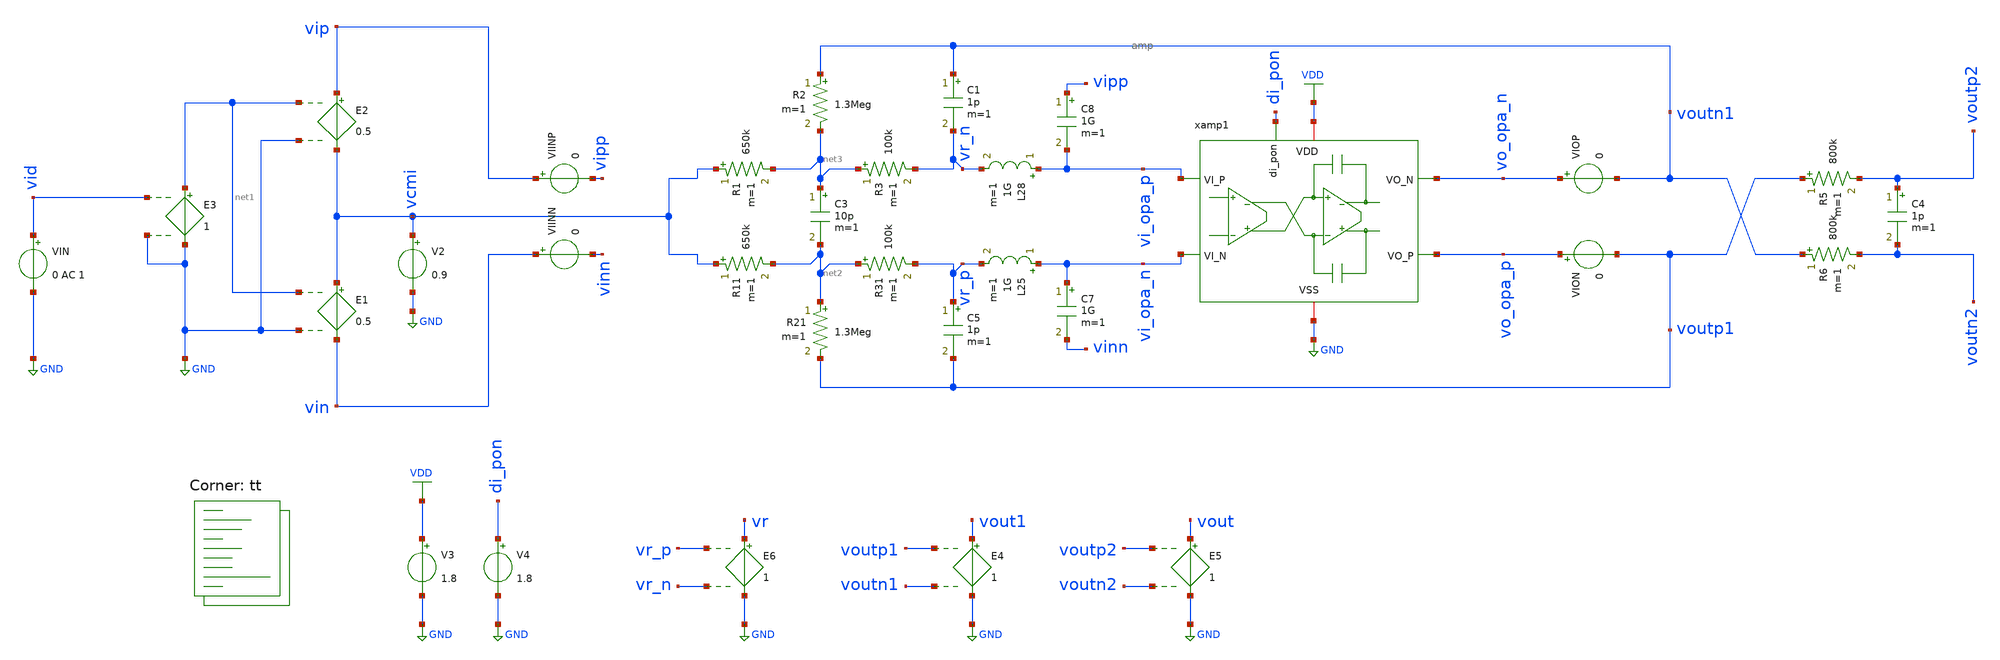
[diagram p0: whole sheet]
** sch_path: xschem/tb_filter_loopgain.sch
**.subckt tb_filter_loopgain
V2 vcmi GND 0.9
E1 vcmi vin net1 GND 0.5
E2 vip vcmi net1 GND 0.5
VIN vid GND 0 AC 1
E3 net1 GND vid GND 1
E4 vout1 GND voutp1 voutn1 1
VIINP vip vipp 0
VIINN vin vinn 0
R1 vcmi net3 650k m=1
R2 voutn1 net3 1.3Meg m=1
R3 net3 vr_n 100k m=1
C1 voutn1 vr_n 1p m=1
C3 net3 net2 10p m=1
R11 vcmi net2 650k m=1
R21 net2 voutp1 1.3Meg m=1
R31 net2 vr_p 100k m=1
C5 vr_p voutp1 1p m=1
E5 vout GND voutp2 voutn2 1
VIOP vo_opa_n voutn1 0
VION vo_opa_p voutp1 0
E6 vr GND vr_p vr_n 1
C7 vi_opa_n vinn 1G m=1
C8 vipp vi_opa_p 1G m=1
L25 vi_opa_n vr_p 1G m=1
L28 vi_opa_p vr_n 1G m=1
xamp1 VDD vi_opa_n vi_opa_p vo_opa_p di_pon vo_opa_n GND amp
V3 VDD GND 1.8
V4 di_pon GND 1.8
C4 voutp2 voutn2 1p m=1
R5 voutp1 voutp2 800k m=1
R6 voutn1 voutn2 800k m=1
**** begin user architecture code
.lib $::SKYWATER_MODELS/sky130.lib.spice tt


.options savecurrents
.options method=gear reltol=.01
.options sparse
.control
save all

let f_sig = 100
let f_min = 10
let f_max = 100G
let f_stop = 5Meg
let tper_sig = 1/f_sig
let tfr_sig = tper_sig/2
let Adc = 10
let beta = 1/Adc
let v_step_o = 0.9
let v_step_i = v_step_o/Adc

let t_rf = 0.1u
let t_step = 50u
let t_delay = 0
let t_per = 2*t_step

let tstep = 0.1*t_rf
let tstop = 2*t_per
let tstart = t_delay

*alter @VIN[SIN] = [ 0 0.01 $&f_sig 0 0 0 ]
alter @VIN[DC] = 0.0

set wr_singlescale
set wr_vecnames
option numdgt=3


** Main Simulations
	op
	ac dec 100 $&const.f_min $&const.f_max

	setplot ac1
	let A1 = v(vout1)/v(vid)
	let A2 = v(vout)/v(vid)
	let L = v(vr)/v(vid)
	let A = L/beta

	let L_re = real(L)
	let L_im = imag(L)

	let L_dB = vdb(L)
	let L_arg = 180/PI*cphase(L)
	let A_dB = vdb(A)
	let A_arg = 180/PI*cphase(A)

	let fdc = const.f_min+1

	meas ac fug find frequency when L_dB=0
	meas ac pm find L_arg when frequency=fug

	let pm = 180-abs(pm)

	print pm

	let err_gain = 1-10^(Adc/20)/10
	let Adc_ol_min = (1-err_gain)/err_gain

	print err_gain
	print Adc_ol_min

	plot L_dB L_arg A_dB A_arg title 'Bode Plot of Loop Gain' ylabel 'Magnitude (dB) / Phase (Deg)'
	plot L_im vs L_re retraceplot title 'Nyquist Plot of Loop Gain' ylabel 'Imaginary Part' xlabel 'Real Part'


alter @VIN[DC] = 0
op

remzerovec
write tb_filter_loopgain.raw
.endc

**** end user architecture code
**.ends
.GLOBAL GND
.GLOBAL VDD
.end
